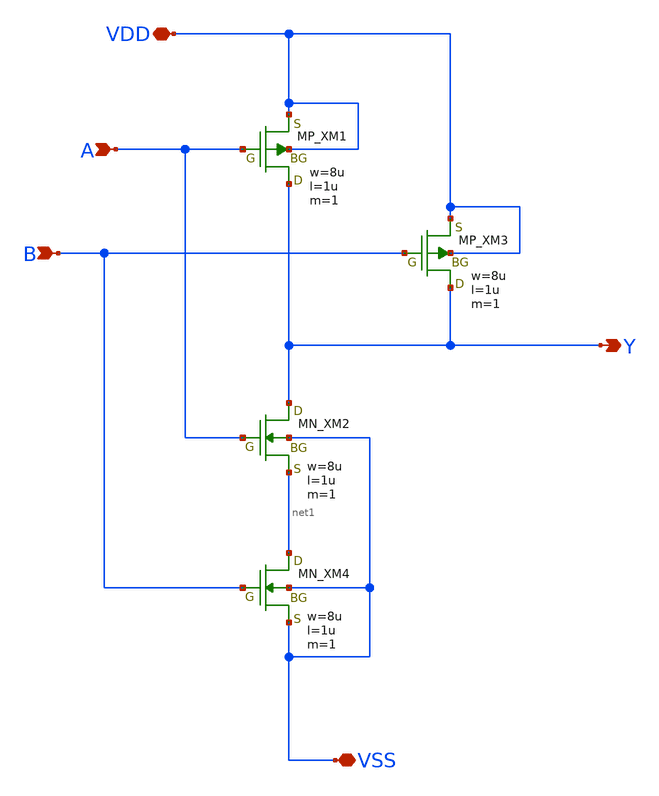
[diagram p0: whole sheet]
** sch_path: src/nand2_regymm.sch
**.subckt nand2_regymm A Y VDD VSS B
*.ipin A
*.opin Y
*.iopin VDD
*.iopin VSS
*.ipin B
XXM1 Y A VDD VDD PMOS w=8u l=1u as=0 ad=0 ps=0 pd=0 nrd=0 nrs=0 m=1
XXM2 Y A net1 VSS NMOS w=8u l=1u as=0 ad=0 ps=0 pd=0 nrd=0 nrs=0 m=1
XXM3 Y B VDD VDD PMOS w=8u l=1u as=0 ad=0 ps=0 pd=0 nrd=0 nrs=0 m=1
XXM4 net1 B VSS VSS NMOS w=8u l=1u as=0 ad=0 ps=0 pd=0 nrd=0 nrs=0 m=1
**.ends
.end
